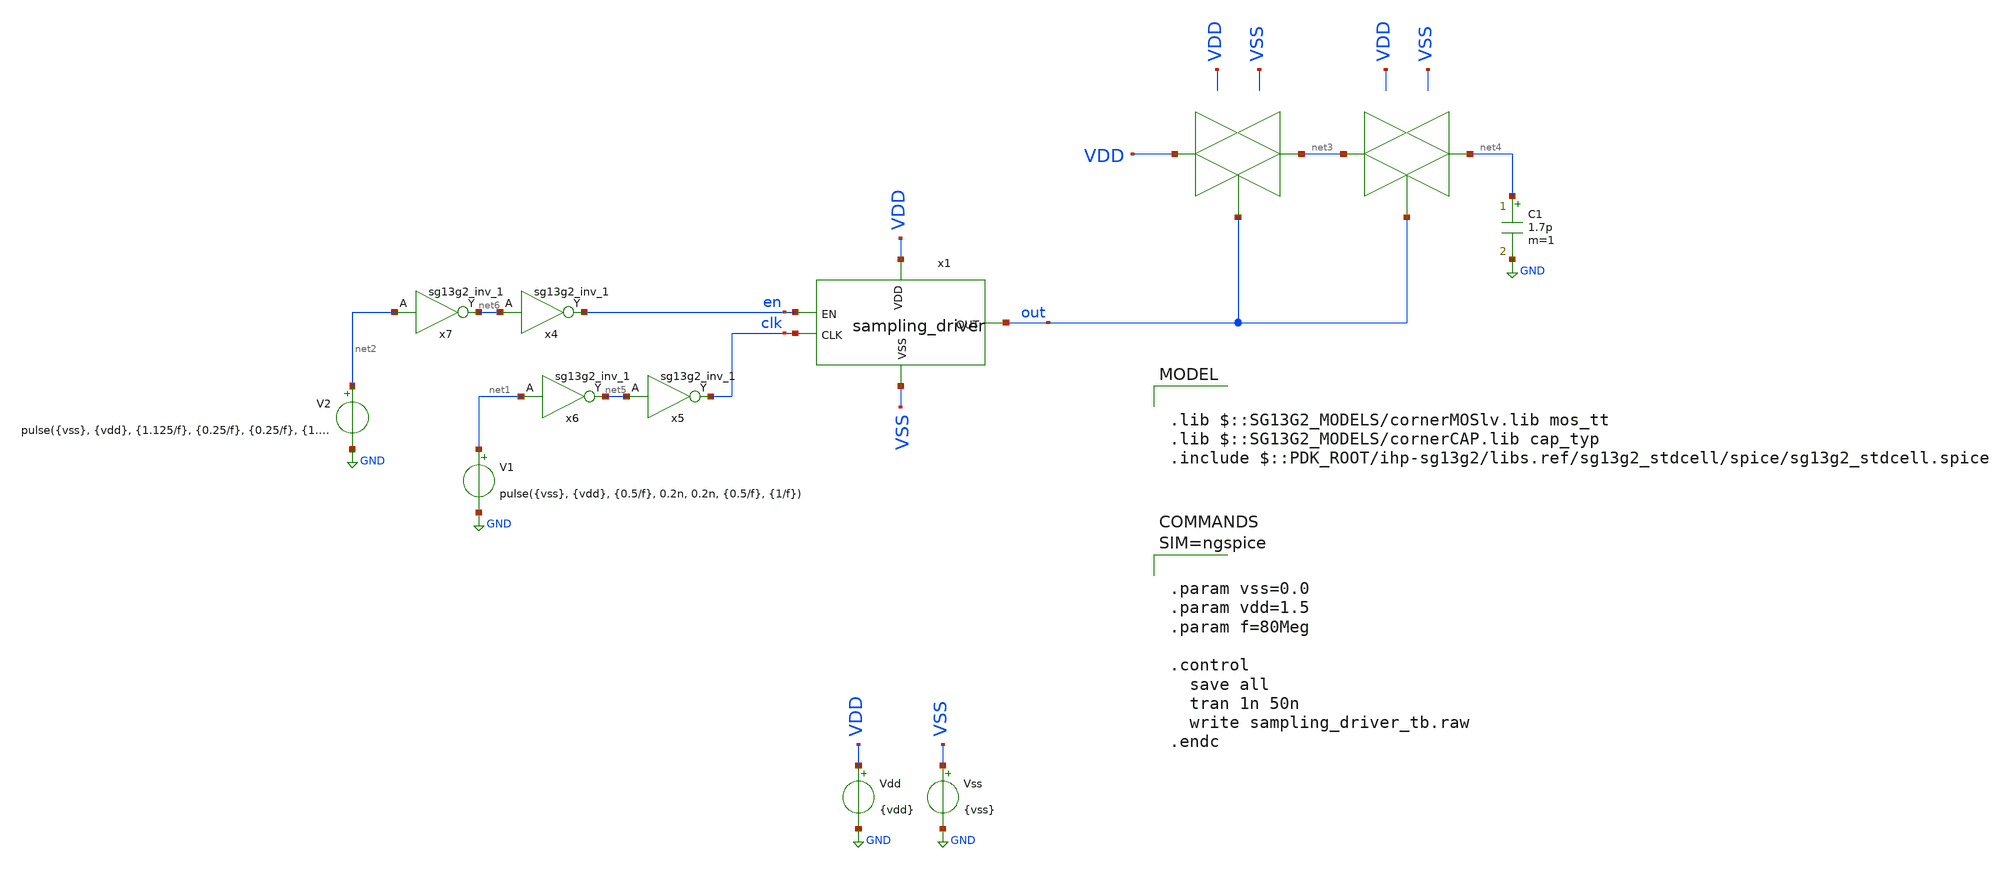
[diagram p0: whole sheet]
** sch_path: designs/sampling_driver/sampling_driver_tb.sch
**.subckt sampling_driver_tb
x1 en out clk VDD VSS sampling_driver
V1 net1 GND pulse({vss}, {vdd}, {0.5/f}, 0.2n, 0.2n, {0.5/f}, {1/f})
V2 net2 GND pulse({vss}, {vdd}, {1.125/f}, {0.25/f}, {0.25/f}, {1.25/f}, {4/f})
C1 net4 GND 1.7p m=1
x4 en net6 VDD VSS sg13g2_inv_1
x5 clk net5 VDD VSS sg13g2_inv_1
x6 net5 net1 VDD VSS sg13g2_inv_1
x7 net6 net2 VDD VSS sg13g2_inv_1
Vdd VDD GND {vdd}
Vss VSS GND {vss}
**** begin user architecture code



.param vss=0.0
.param vdd=1.5
.param f=80Meg

.control
  save all
  tran 1n 50n
  write sampling_driver_tb.raw
.endc




.lib $::SG13G2_MODELS/cornerMOSlv.lib mos_tt
.lib $::SG13G2_MODELS/cornerCAP.lib cap_typ
.include $::PDK_ROOT/ihp-sg13g2/libs.ref/sg13g2_stdcell/spice/sg13g2_stdcell.spice

**** end user architecture code
**.ends

* expanding   symbol:  sampling_driver.sym # of pins=5
** sym_path: designs/sampling_driver/sampling_driver.sym
** sch_path: designs/sampling_driver/sampling_driver.sch
.subckt sampling_driver EN OUT CLK VDD VSS
*.ipin CLK
*.ipin EN
*.opin OUT
*.ipin VDD
*.ipin VSS
XM1 net4 CLK VDD VDD sg13_lv_pmos w=0.15u l=0.13u ng=1 m=1 mm_ok=1
XM2 net2 net1 net4 VDD sg13_lv_pmos w=0.15u l=0.13u ng=1 m=1 mm_ok=1
XM3 net2 EN net3 VSS sg13_lv_nmos w=0.15u l=0.13u ng=1 m=1 mm_ok=1
XM4 net3 CLK VSS VSS sg13_lv_nmos w=0.15u l=0.13u ng=1 m=1 mm_ok=1
x1 net1 EN VDD VSS sg13g2_inv_1
XM5 net2 net1 VSS VSS sg13_lv_nmos w=0.15u l=0.13u ng=1 m=1 mm_ok=1
x2 OUT net2 VDD VSS sg13g2_inv_1
.ends


* expanding   symbol:  sg13g2_stdcells/sg13g2_inv_1.sym # of pins=2
** sym_path: sg13g2_stdcells/sg13g2_inv_1.sym
** sch_path: sg13g2_stdcells/sg13g2_inv_1.sch
.subckt sg13g2_inv_1 Y A VDD VSS
*.opin Y
*.ipin A
*.iopin VDD
*.iopin VSS
XM1 Y A VSS VSS sg13_lv_nmos w=740.00n l=130.00n ng=1 m=1 mm_ok=1
XM2 Y A VDD VDD sg13_lv_pmos w=1.12u l=130.00n ng=1 m=1 mm_ok=1
.ends

.GLOBAL GND
.end
